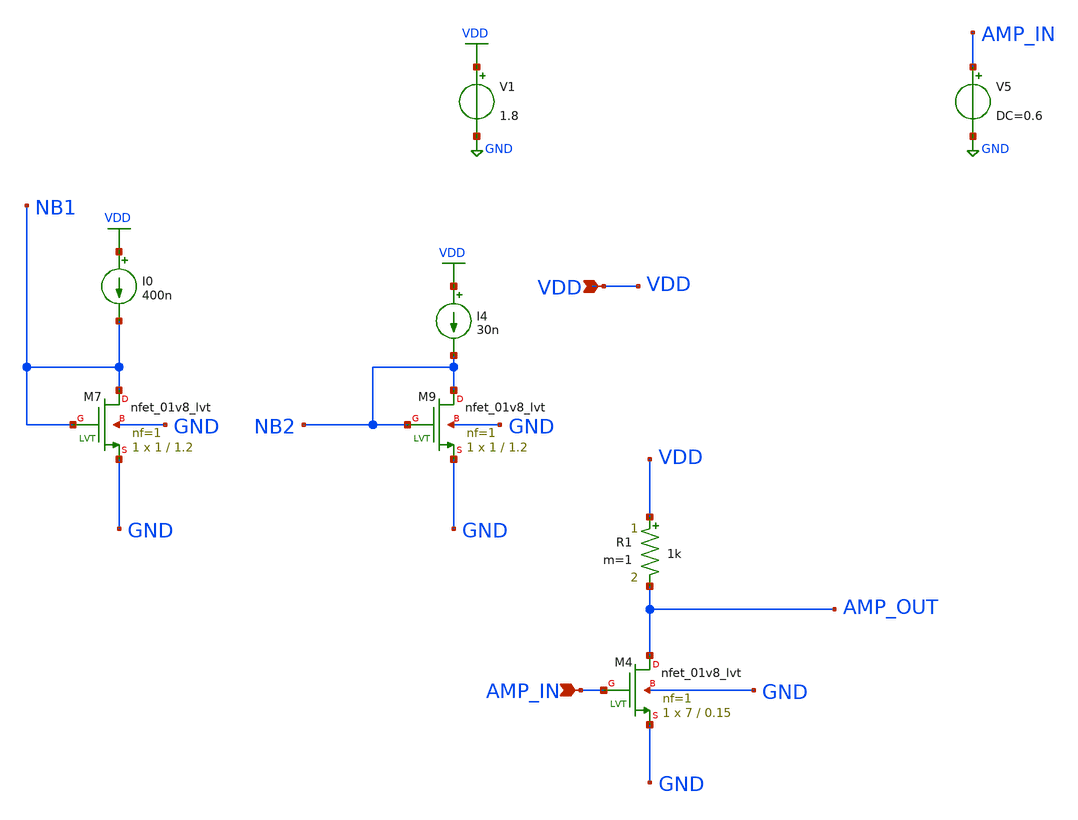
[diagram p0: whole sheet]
** sch_path: xschem/untitled-1.sch
**.subckt untitled-1 AMP_IN VDD
*.ipin AMP_IN
*.ipin VDD
V1 VDD GND 1.8
XM4 AMP_OUT AMP_IN GND GND sky130_fd_pr__nfet_01v8_lvt L=0.15 W=7 nf=1 ad='int((nf+1)/2) * W/nf * 0.29'
+ as='int((nf+2)/2) * W/nf * 0.29' pd='2*int((nf+1)/2) * (W/nf + 0.29)' ps='2*int((nf+2)/2) * (W/nf + 0.29)'
+ nrd='0.29 / W' nrs='0.29 / W' sa=0 sb=0 sd=0 mult=1 m=1
XM7 NB1 NB1 GND GND sky130_fd_pr__nfet_01v8_lvt L=1.2 W=1 nf=1 ad='int((nf+1)/2) * W/nf * 0.29' as='int((nf+2)/2) * W/nf * 0.29'
+ pd='2*int((nf+1)/2) * (W/nf + 0.29)' ps='2*int((nf+2)/2) * (W/nf + 0.29)' nrd='0.29 / W' nrs='0.29 / W'
+ sa=0 sb=0 sd=0 mult=1 m=1
I0 VDD NB1 400n
I4 VDD NB2 30n
XM9 NB2 NB2 GND GND sky130_fd_pr__nfet_01v8_lvt L=1.2 W=1 nf=1 ad='int((nf+1)/2) * W/nf * 0.29' as='int((nf+2)/2) * W/nf * 0.29'
+ pd='2*int((nf+1)/2) * (W/nf + 0.29)' ps='2*int((nf+2)/2) * (W/nf + 0.29)' nrd='0.29 / W' nrs='0.29 / W'
+ sa=0 sb=0 sd=0 mult=1 m=1
V5 AMP_IN GND DC=0.6
R1 VDD AMP_OUT 1k m=1
**** begin user architecture code

** opencircuitdesign pdks install
.lib $::SKYWATER_MODELS/sky130.lib.spice tt


**** end user architecture code
**.ends
.GLOBAL GND
.GLOBAL VDD
**** begin user architecture code


.options gmin=0.0000000000000000000001
*.options savecurrents

.control
save all

*tran 1m 50m
*plot v(test)
DC V5 0.2 0.8 0.001
plot v(amp_out)

*noise v(PIX_OUT) V8 dec 10 1 1Meg
*setplot noise2
*print onoise_total

*noise v(PIX_OUT) V8 dec 10 1 1Meg
*setplot noise2
*print onoise_total
.endc


**** end user architecture code
.end
